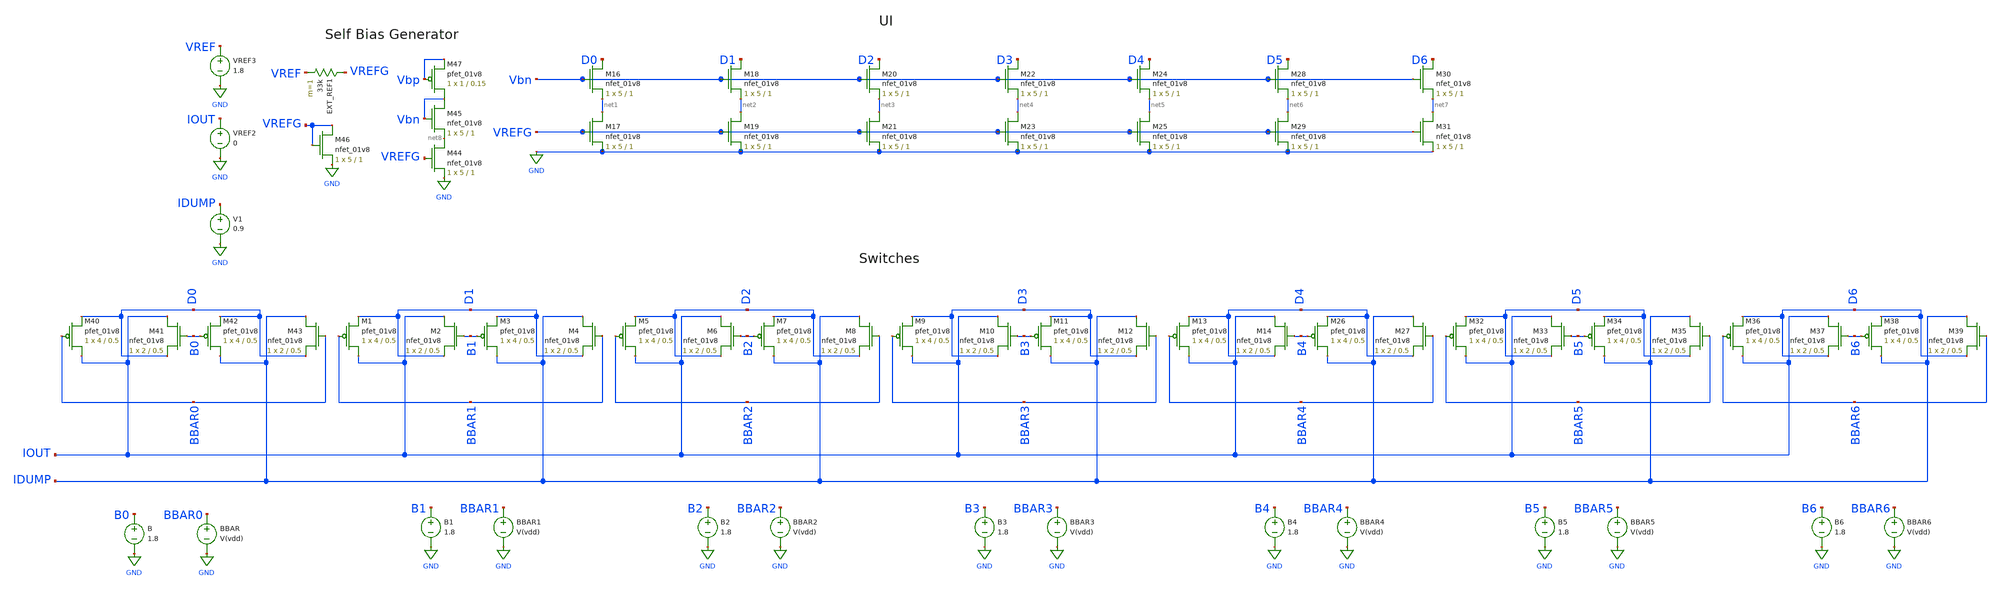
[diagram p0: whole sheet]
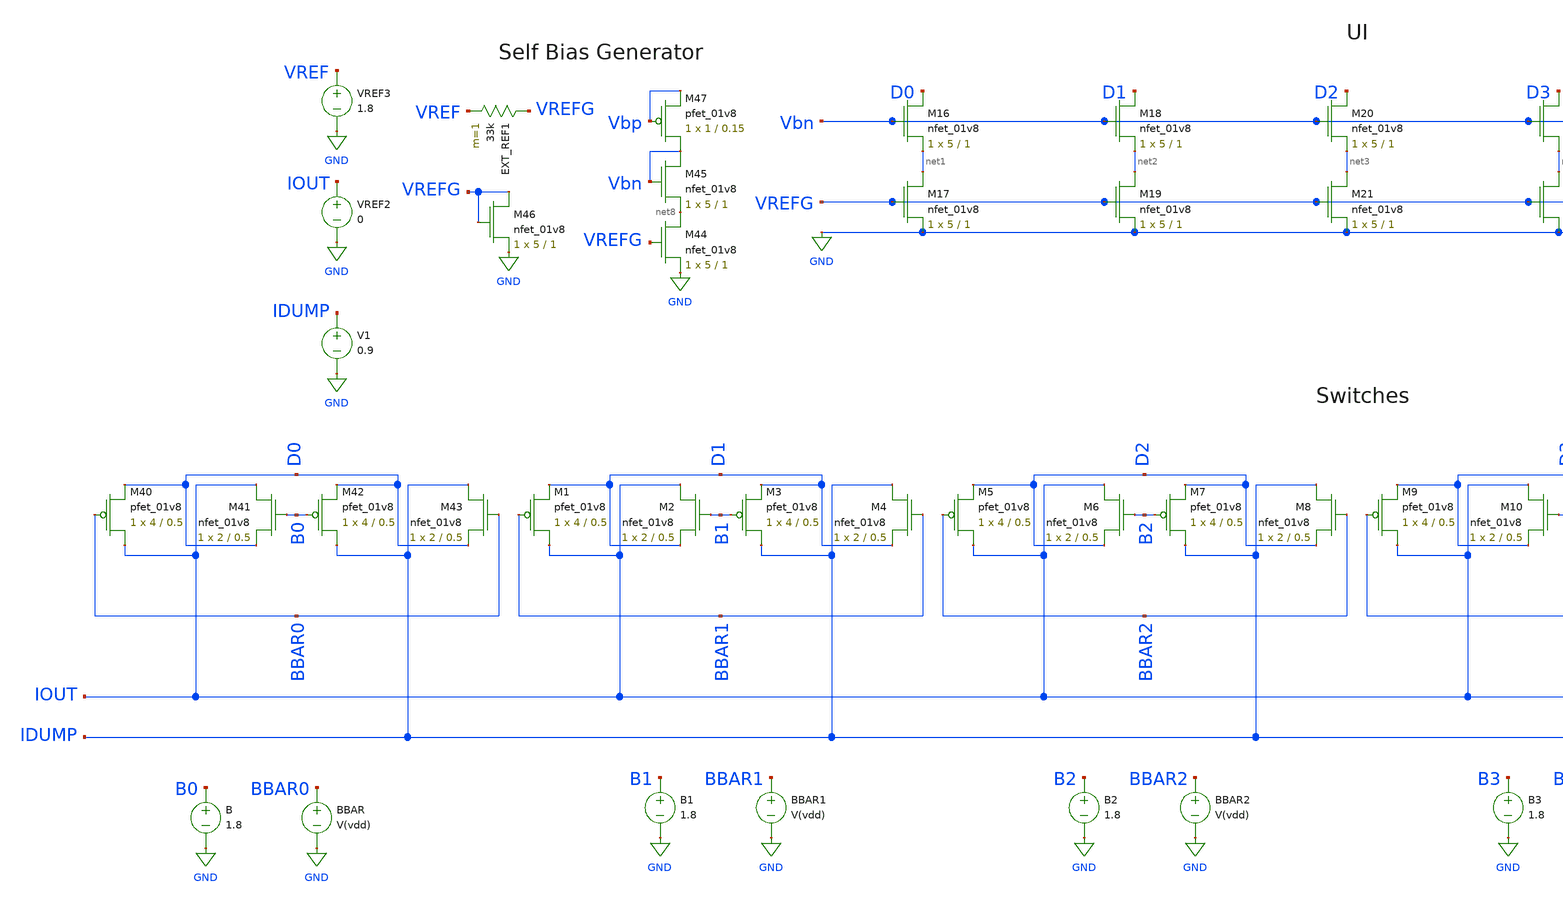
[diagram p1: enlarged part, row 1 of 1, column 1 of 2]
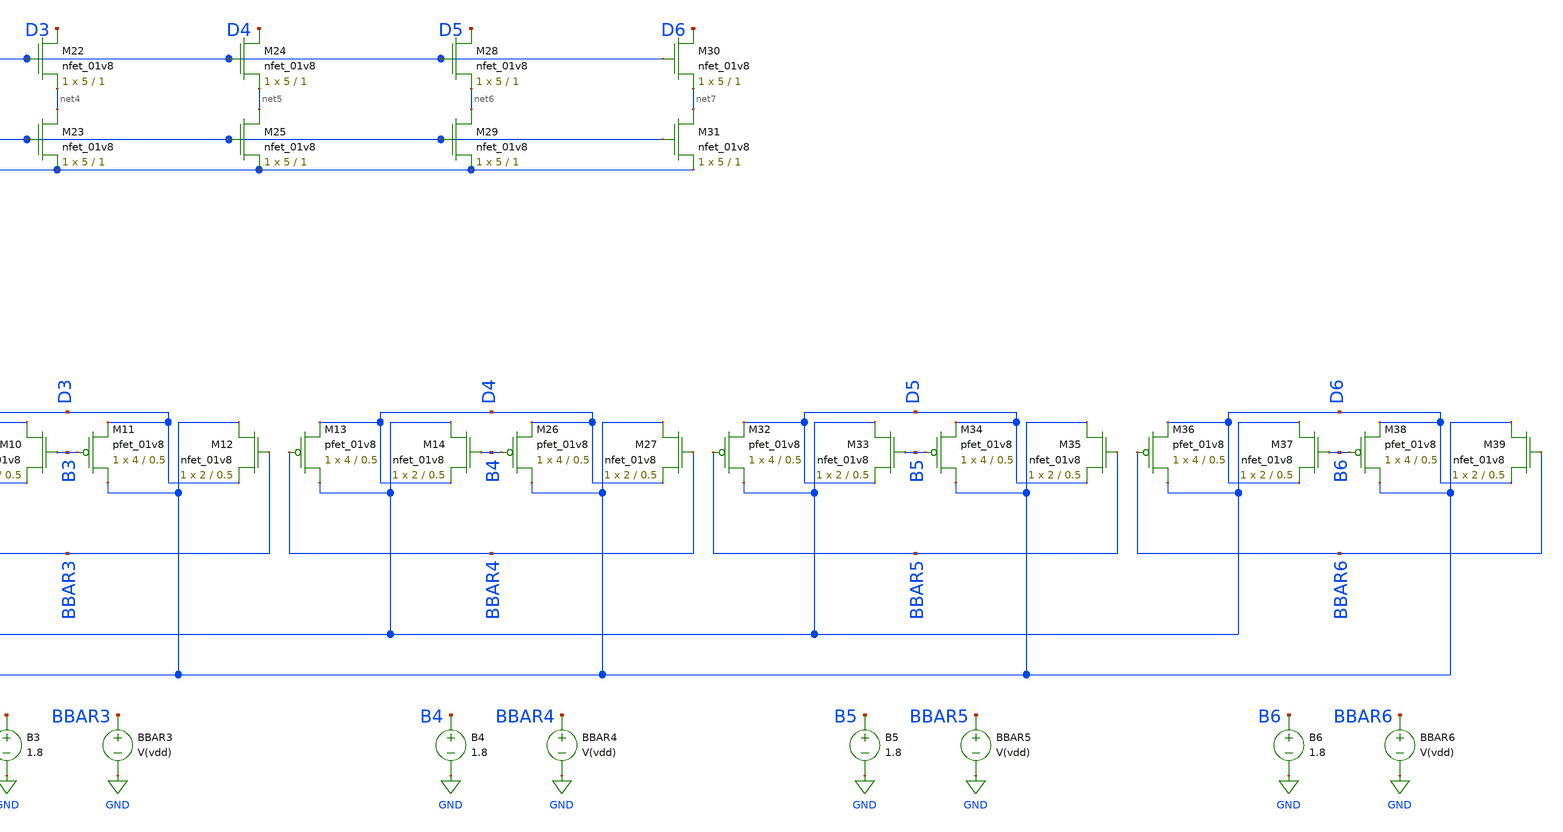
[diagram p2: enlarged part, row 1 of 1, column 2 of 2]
** sch_path: DAC2.sch
**.subckt DAC2
XM16 D0 Vbn net1 GND sky130_fd_pr__nfet_01v8 L=1 W=5 nf=1 ad='int((nf+1)/2) * W/nf * 0.29' as='int((nf+2)/2) * W/nf * 0.29'
+ pd='2*int((nf+1)/2) * (W/nf + 0.29)' ps='2*int((nf+2)/2) * (W/nf + 0.29)' nrd='0.29 / W' nrs='0.29 / W'
+ sa=0 sb=0 sd=0 mult=1 m=1
XM17 net1 VREFG GND GND sky130_fd_pr__nfet_01v8 L=1 W=5 nf=1 ad='int((nf+1)/2) * W/nf * 0.29' as='int((nf+2)/2) * W/nf * 0.29'
+ pd='2*int((nf+1)/2) * (W/nf + 0.29)' ps='2*int((nf+2)/2) * (W/nf + 0.29)' nrd='0.29 / W' nrs='0.29 / W'
+ sa=0 sb=0 sd=0 mult=1 m=1
XM18 D1 Vbn net2 GND sky130_fd_pr__nfet_01v8 L=1 W=5 nf=1 ad='int((nf+1)/2) * W/nf * 0.29' as='int((nf+2)/2) * W/nf * 0.29'
+ pd='2*int((nf+1)/2) * (W/nf + 0.29)' ps='2*int((nf+2)/2) * (W/nf + 0.29)' nrd='0.29 / W' nrs='0.29 / W'
+ sa=0 sb=0 sd=0 mult=1 m=1
XM19 net2 VREFG GND GND sky130_fd_pr__nfet_01v8 L=1 W=5 nf=1 ad='int((nf+1)/2) * W/nf * 0.29' as='int((nf+2)/2) * W/nf * 0.29'
+ pd='2*int((nf+1)/2) * (W/nf + 0.29)' ps='2*int((nf+2)/2) * (W/nf + 0.29)' nrd='0.29 / W' nrs='0.29 / W'
+ sa=0 sb=0 sd=0 mult=1 m=1
XM20 D2 Vbn net3 GND sky130_fd_pr__nfet_01v8 L=1 W=5 nf=1 ad='int((nf+1)/2) * W/nf * 0.29' as='int((nf+2)/2) * W/nf * 0.29'
+ pd='2*int((nf+1)/2) * (W/nf + 0.29)' ps='2*int((nf+2)/2) * (W/nf + 0.29)' nrd='0.29 / W' nrs='0.29 / W'
+ sa=0 sb=0 sd=0 mult=1 m=1
XM21 net3 VREFG GND GND sky130_fd_pr__nfet_01v8 L=1 W=5 nf=1 ad='int((nf+1)/2) * W/nf * 0.29' as='int((nf+2)/2) * W/nf * 0.29'
+ pd='2*int((nf+1)/2) * (W/nf + 0.29)' ps='2*int((nf+2)/2) * (W/nf + 0.29)' nrd='0.29 / W' nrs='0.29 / W'
+ sa=0 sb=0 sd=0 mult=1 m=1
XM22 D3 Vbn net4 GND sky130_fd_pr__nfet_01v8 L=1 W=5 nf=1 ad='int((nf+1)/2) * W/nf * 0.29' as='int((nf+2)/2) * W/nf * 0.29'
+ pd='2*int((nf+1)/2) * (W/nf + 0.29)' ps='2*int((nf+2)/2) * (W/nf + 0.29)' nrd='0.29 / W' nrs='0.29 / W'
+ sa=0 sb=0 sd=0 mult=1 m=1
XM23 net4 VREFG GND GND sky130_fd_pr__nfet_01v8 L=1 W=5 nf=1 ad='int((nf+1)/2) * W/nf * 0.29' as='int((nf+2)/2) * W/nf * 0.29'
+ pd='2*int((nf+1)/2) * (W/nf + 0.29)' ps='2*int((nf+2)/2) * (W/nf + 0.29)' nrd='0.29 / W' nrs='0.29 / W'
+ sa=0 sb=0 sd=0 mult=1 m=1
XM24 D4 Vbn net5 GND sky130_fd_pr__nfet_01v8 L=1 W=5 nf=1 ad='int((nf+1)/2) * W/nf * 0.29' as='int((nf+2)/2) * W/nf * 0.29'
+ pd='2*int((nf+1)/2) * (W/nf + 0.29)' ps='2*int((nf+2)/2) * (W/nf + 0.29)' nrd='0.29 / W' nrs='0.29 / W'
+ sa=0 sb=0 sd=0 mult=1 m=1
XM25 net5 VREFG GND GND sky130_fd_pr__nfet_01v8 L=1 W=5 nf=1 ad='int((nf+1)/2) * W/nf * 0.29' as='int((nf+2)/2) * W/nf * 0.29'
+ pd='2*int((nf+1)/2) * (W/nf + 0.29)' ps='2*int((nf+2)/2) * (W/nf + 0.29)' nrd='0.29 / W' nrs='0.29 / W'
+ sa=0 sb=0 sd=0 mult=1 m=1
XM28 D5 Vbn net6 GND sky130_fd_pr__nfet_01v8 L=1 W=5 nf=1 ad='int((nf+1)/2) * W/nf * 0.29' as='int((nf+2)/2) * W/nf * 0.29'
+ pd='2*int((nf+1)/2) * (W/nf + 0.29)' ps='2*int((nf+2)/2) * (W/nf + 0.29)' nrd='0.29 / W' nrs='0.29 / W'
+ sa=0 sb=0 sd=0 mult=1 m=1
XM29 net6 VREFG GND GND sky130_fd_pr__nfet_01v8 L=1 W=5 nf=1 ad='int((nf+1)/2) * W/nf * 0.29' as='int((nf+2)/2) * W/nf * 0.29'
+ pd='2*int((nf+1)/2) * (W/nf + 0.29)' ps='2*int((nf+2)/2) * (W/nf + 0.29)' nrd='0.29 / W' nrs='0.29 / W'
+ sa=0 sb=0 sd=0 mult=1 m=1
XM30 D6 Vbn net7 GND sky130_fd_pr__nfet_01v8 L=1 W=5 nf=1 ad='int((nf+1)/2) * W/nf * 0.29' as='int((nf+2)/2) * W/nf * 0.29'
+ pd='2*int((nf+1)/2) * (W/nf + 0.29)' ps='2*int((nf+2)/2) * (W/nf + 0.29)' nrd='0.29 / W' nrs='0.29 / W'
+ sa=0 sb=0 sd=0 mult=1 m=1
XM31 net7 VREFG GND GND sky130_fd_pr__nfet_01v8 L=1 W=5 nf=1 ad='int((nf+1)/2) * W/nf * 0.29' as='int((nf+2)/2) * W/nf * 0.29'
+ pd='2*int((nf+1)/2) * (W/nf + 0.29)' ps='2*int((nf+2)/2) * (W/nf + 0.29)' nrd='0.29 / W' nrs='0.29 / W'
+ sa=0 sb=0 sd=0 mult=1 m=1
VREF2 IOUT GND 0
XM1 IOUT BBAR1 D1 VDD sky130_fd_pr__pfet_01v8 L=0.5 W=4 nf=1 ad='int((nf+1)/2) * W/nf * 0.29' as='int((nf+2)/2) * W/nf * 0.29'
+ pd='2*int((nf+1)/2) * (W/nf + 0.29)' ps='2*int((nf+2)/2) * (W/nf + 0.29)' nrd='0.29 / W' nrs='0.29 / W'
+ sa=0 sb=0 sd=0 mult=1 m=1
XM2 IOUT B1 D1 GND sky130_fd_pr__nfet_01v8 L=0.5 W=2 nf=1 ad='int((nf+1)/2) * W/nf * 0.29' as='int((nf+2)/2) * W/nf * 0.29'
+ pd='2*int((nf+1)/2) * (W/nf + 0.29)' ps='2*int((nf+2)/2) * (W/nf + 0.29)' nrd='0.29 / W' nrs='0.29 / W'
+ sa=0 sb=0 sd=0 mult=1 m=1
XM3 IDUMP B1 D1 VDD sky130_fd_pr__pfet_01v8 L=0.5 W=4 nf=1 ad='int((nf+1)/2) * W/nf * 0.29' as='int((nf+2)/2) * W/nf * 0.29'
+ pd='2*int((nf+1)/2) * (W/nf + 0.29)' ps='2*int((nf+2)/2) * (W/nf + 0.29)' nrd='0.29 / W' nrs='0.29 / W'
+ sa=0 sb=0 sd=0 mult=1 m=1
XM4 IDUMP BBAR1 D1 GND sky130_fd_pr__nfet_01v8 L=0.5 W=2 nf=1 ad='int((nf+1)/2) * W/nf * 0.29' as='int((nf+2)/2) * W/nf * 0.29'
+ pd='2*int((nf+1)/2) * (W/nf + 0.29)' ps='2*int((nf+2)/2) * (W/nf + 0.29)' nrd='0.29 / W' nrs='0.29 / W'
+ sa=0 sb=0 sd=0 mult=1 m=1
V1 IDUMP GND 0.9
XM5 IOUT BBAR2 D2 VDD sky130_fd_pr__pfet_01v8 L=0.5 W=4 nf=1 ad='int((nf+1)/2) * W/nf * 0.29' as='int((nf+2)/2) * W/nf * 0.29'
+ pd='2*int((nf+1)/2) * (W/nf + 0.29)' ps='2*int((nf+2)/2) * (W/nf + 0.29)' nrd='0.29 / W' nrs='0.29 / W'
+ sa=0 sb=0 sd=0 mult=1 m=1
XM6 IOUT B2 D2 GND sky130_fd_pr__nfet_01v8 L=0.5 W=2 nf=1 ad='int((nf+1)/2) * W/nf * 0.29' as='int((nf+2)/2) * W/nf * 0.29'
+ pd='2*int((nf+1)/2) * (W/nf + 0.29)' ps='2*int((nf+2)/2) * (W/nf + 0.29)' nrd='0.29 / W' nrs='0.29 / W'
+ sa=0 sb=0 sd=0 mult=1 m=1
XM7 IDUMP B2 D2 VDD sky130_fd_pr__pfet_01v8 L=0.5 W=4 nf=1 ad='int((nf+1)/2) * W/nf * 0.29' as='int((nf+2)/2) * W/nf * 0.29'
+ pd='2*int((nf+1)/2) * (W/nf + 0.29)' ps='2*int((nf+2)/2) * (W/nf + 0.29)' nrd='0.29 / W' nrs='0.29 / W'
+ sa=0 sb=0 sd=0 mult=1 m=1
XM8 IDUMP BBAR2 D2 GND sky130_fd_pr__nfet_01v8 L=0.5 W=2 nf=1 ad='int((nf+1)/2) * W/nf * 0.29' as='int((nf+2)/2) * W/nf * 0.29'
+ pd='2*int((nf+1)/2) * (W/nf + 0.29)' ps='2*int((nf+2)/2) * (W/nf + 0.29)' nrd='0.29 / W' nrs='0.29 / W'
+ sa=0 sb=0 sd=0 mult=1 m=1
XM9 IOUT BBAR3 D3 VDD sky130_fd_pr__pfet_01v8 L=0.5 W=4 nf=1 ad='int((nf+1)/2) * W/nf * 0.29' as='int((nf+2)/2) * W/nf * 0.29'
+ pd='2*int((nf+1)/2) * (W/nf + 0.29)' ps='2*int((nf+2)/2) * (W/nf + 0.29)' nrd='0.29 / W' nrs='0.29 / W'
+ sa=0 sb=0 sd=0 mult=1 m=1
XM10 IOUT B3 D3 GND sky130_fd_pr__nfet_01v8 L=0.5 W=2 nf=1 ad='int((nf+1)/2) * W/nf * 0.29' as='int((nf+2)/2) * W/nf * 0.29'
+ pd='2*int((nf+1)/2) * (W/nf + 0.29)' ps='2*int((nf+2)/2) * (W/nf + 0.29)' nrd='0.29 / W' nrs='0.29 / W'
+ sa=0 sb=0 sd=0 mult=1 m=1
XM11 IDUMP B3 D3 VDD sky130_fd_pr__pfet_01v8 L=0.5 W=4 nf=1 ad='int((nf+1)/2) * W/nf * 0.29' as='int((nf+2)/2) * W/nf * 0.29'
+ pd='2*int((nf+1)/2) * (W/nf + 0.29)' ps='2*int((nf+2)/2) * (W/nf + 0.29)' nrd='0.29 / W' nrs='0.29 / W'
+ sa=0 sb=0 sd=0 mult=1 m=1
XM12 IDUMP BBAR3 D3 GND sky130_fd_pr__nfet_01v8 L=0.5 W=2 nf=1 ad='int((nf+1)/2) * W/nf * 0.29' as='int((nf+2)/2) * W/nf * 0.29'
+ pd='2*int((nf+1)/2) * (W/nf + 0.29)' ps='2*int((nf+2)/2) * (W/nf + 0.29)' nrd='0.29 / W' nrs='0.29 / W'
+ sa=0 sb=0 sd=0 mult=1 m=1
XM13 IOUT BBAR4 D4 VDD sky130_fd_pr__pfet_01v8 L=0.5 W=4 nf=1 ad='int((nf+1)/2) * W/nf * 0.29' as='int((nf+2)/2) * W/nf * 0.29'
+ pd='2*int((nf+1)/2) * (W/nf + 0.29)' ps='2*int((nf+2)/2) * (W/nf + 0.29)' nrd='0.29 / W' nrs='0.29 / W'
+ sa=0 sb=0 sd=0 mult=1 m=1
XM14 IOUT B4 D4 GND sky130_fd_pr__nfet_01v8 L=0.5 W=2 nf=1 ad='int((nf+1)/2) * W/nf * 0.29' as='int((nf+2)/2) * W/nf * 0.29'
+ pd='2*int((nf+1)/2) * (W/nf + 0.29)' ps='2*int((nf+2)/2) * (W/nf + 0.29)' nrd='0.29 / W' nrs='0.29 / W'
+ sa=0 sb=0 sd=0 mult=1 m=1
XM26 IDUMP B4 D4 VDD sky130_fd_pr__pfet_01v8 L=0.5 W=4 nf=1 ad='int((nf+1)/2) * W/nf * 0.29' as='int((nf+2)/2) * W/nf * 0.29'
+ pd='2*int((nf+1)/2) * (W/nf + 0.29)' ps='2*int((nf+2)/2) * (W/nf + 0.29)' nrd='0.29 / W' nrs='0.29 / W'
+ sa=0 sb=0 sd=0 mult=1 m=1
XM27 IDUMP BBAR4 D4 GND sky130_fd_pr__nfet_01v8 L=0.5 W=2 nf=1 ad='int((nf+1)/2) * W/nf * 0.29' as='int((nf+2)/2) * W/nf * 0.29'
+ pd='2*int((nf+1)/2) * (W/nf + 0.29)' ps='2*int((nf+2)/2) * (W/nf + 0.29)' nrd='0.29 / W' nrs='0.29 / W'
+ sa=0 sb=0 sd=0 mult=1 m=1
XM32 IOUT BBAR5 D5 VDD sky130_fd_pr__pfet_01v8 L=0.5 W=4 nf=1 ad='int((nf+1)/2) * W/nf * 0.29' as='int((nf+2)/2) * W/nf * 0.29'
+ pd='2*int((nf+1)/2) * (W/nf + 0.29)' ps='2*int((nf+2)/2) * (W/nf + 0.29)' nrd='0.29 / W' nrs='0.29 / W'
+ sa=0 sb=0 sd=0 mult=1 m=1
XM33 IOUT B5 D5 GND sky130_fd_pr__nfet_01v8 L=0.5 W=2 nf=1 ad='int((nf+1)/2) * W/nf * 0.29' as='int((nf+2)/2) * W/nf * 0.29'
+ pd='2*int((nf+1)/2) * (W/nf + 0.29)' ps='2*int((nf+2)/2) * (W/nf + 0.29)' nrd='0.29 / W' nrs='0.29 / W'
+ sa=0 sb=0 sd=0 mult=1 m=1
XM34 IDUMP B5 D5 VDD sky130_fd_pr__pfet_01v8 L=0.5 W=4 nf=1 ad='int((nf+1)/2) * W/nf * 0.29' as='int((nf+2)/2) * W/nf * 0.29'
+ pd='2*int((nf+1)/2) * (W/nf + 0.29)' ps='2*int((nf+2)/2) * (W/nf + 0.29)' nrd='0.29 / W' nrs='0.29 / W'
+ sa=0 sb=0 sd=0 mult=1 m=1
XM35 IDUMP BBAR5 D5 GND sky130_fd_pr__nfet_01v8 L=0.5 W=2 nf=1 ad='int((nf+1)/2) * W/nf * 0.29' as='int((nf+2)/2) * W/nf * 0.29'
+ pd='2*int((nf+1)/2) * (W/nf + 0.29)' ps='2*int((nf+2)/2) * (W/nf + 0.29)' nrd='0.29 / W' nrs='0.29 / W'
+ sa=0 sb=0 sd=0 mult=1 m=1
XM36 IOUT BBAR6 D6 VDD sky130_fd_pr__pfet_01v8 L=0.5 W=4 nf=1 ad='int((nf+1)/2) * W/nf * 0.29' as='int((nf+2)/2) * W/nf * 0.29'
+ pd='2*int((nf+1)/2) * (W/nf + 0.29)' ps='2*int((nf+2)/2) * (W/nf + 0.29)' nrd='0.29 / W' nrs='0.29 / W'
+ sa=0 sb=0 sd=0 mult=1 m=1
XM37 IOUT B6 D6 GND sky130_fd_pr__nfet_01v8 L=0.5 W=2 nf=1 ad='int((nf+1)/2) * W/nf * 0.29' as='int((nf+2)/2) * W/nf * 0.29'
+ pd='2*int((nf+1)/2) * (W/nf + 0.29)' ps='2*int((nf+2)/2) * (W/nf + 0.29)' nrd='0.29 / W' nrs='0.29 / W'
+ sa=0 sb=0 sd=0 mult=1 m=1
XM38 IDUMP B6 D6 VDD sky130_fd_pr__pfet_01v8 L=0.5 W=4 nf=1 ad='int((nf+1)/2) * W/nf * 0.29' as='int((nf+2)/2) * W/nf * 0.29'
+ pd='2*int((nf+1)/2) * (W/nf + 0.29)' ps='2*int((nf+2)/2) * (W/nf + 0.29)' nrd='0.29 / W' nrs='0.29 / W'
+ sa=0 sb=0 sd=0 mult=1 m=1
XM39 IDUMP BBAR6 D6 GND sky130_fd_pr__nfet_01v8 L=0.5 W=2 nf=1 ad='int((nf+1)/2) * W/nf * 0.29' as='int((nf+2)/2) * W/nf * 0.29'
+ pd='2*int((nf+1)/2) * (W/nf + 0.29)' ps='2*int((nf+2)/2) * (W/nf + 0.29)' nrd='0.29 / W' nrs='0.29 / W'
+ sa=0 sb=0 sd=0 mult=1 m=1
XM40 IOUT BBAR0 D0 VDD sky130_fd_pr__pfet_01v8 L=0.5 W=4 nf=1 ad='int((nf+1)/2) * W/nf * 0.29' as='int((nf+2)/2) * W/nf * 0.29'
+ pd='2*int((nf+1)/2) * (W/nf + 0.29)' ps='2*int((nf+2)/2) * (W/nf + 0.29)' nrd='0.29 / W' nrs='0.29 / W'
+ sa=0 sb=0 sd=0 mult=1 m=1
XM41 IOUT B0 D0 GND sky130_fd_pr__nfet_01v8 L=0.5 W=2 nf=1 ad='int((nf+1)/2) * W/nf * 0.29' as='int((nf+2)/2) * W/nf * 0.29'
+ pd='2*int((nf+1)/2) * (W/nf + 0.29)' ps='2*int((nf+2)/2) * (W/nf + 0.29)' nrd='0.29 / W' nrs='0.29 / W'
+ sa=0 sb=0 sd=0 mult=1 m=1
XM42 IDUMP B0 D0 VDD sky130_fd_pr__pfet_01v8 L=0.5 W=4 nf=1 ad='int((nf+1)/2) * W/nf * 0.29' as='int((nf+2)/2) * W/nf * 0.29'
+ pd='2*int((nf+1)/2) * (W/nf + 0.29)' ps='2*int((nf+2)/2) * (W/nf + 0.29)' nrd='0.29 / W' nrs='0.29 / W'
+ sa=0 sb=0 sd=0 mult=1 m=1
XM43 IDUMP BBAR0 D0 GND sky130_fd_pr__nfet_01v8 L=0.5 W=2 nf=1 ad='int((nf+1)/2) * W/nf * 0.29' as='int((nf+2)/2) * W/nf * 0.29'
+ pd='2*int((nf+1)/2) * (W/nf + 0.29)' ps='2*int((nf+2)/2) * (W/nf + 0.29)' nrd='0.29 / W' nrs='0.29 / W'
+ sa=0 sb=0 sd=0 mult=1 m=1
B B0 GND 1.8
BBAR BBAR0 GND V(vdd)
B1 B1 GND 1.8
BBAR1 BBAR1 GND V(vdd)
B2 B2 GND 1.8
BBAR2 BBAR2 GND V(vdd)
B3 B3 GND 1.8
BBAR3 BBAR3 GND V(vdd)
B4 B4 GND 1.8
BBAR4 BBAR4 GND V(vdd)
B5 B5 GND 1.8
BBAR5 BBAR5 GND V(vdd)
B6 B6 GND 1.8
BBAR6 BBAR6 GND V(vdd)
XM44 net8 VREFG GND GND sky130_fd_pr__nfet_01v8 L=1 W=5 nf=1 ad='int((nf+1)/2) * W/nf * 0.29' as='int((nf+2)/2) * W/nf * 0.29'
+ pd='2*int((nf+1)/2) * (W/nf + 0.29)' ps='2*int((nf+2)/2) * (W/nf + 0.29)' nrd='0.29 / W' nrs='0.29 / W'
+ sa=0 sb=0 sd=0 mult=1 m=1
EXT_REF1 VREFG VREF 33k m=1
VREF3 VREF GND 1.8
XM45 Vbn Vbn net8 GND sky130_fd_pr__nfet_01v8 L=1 W=5 nf=1 ad='int((nf+1)/2) * W/nf * 0.29' as='int((nf+2)/2) * W/nf * 0.29'
+ pd='2*int((nf+1)/2) * (W/nf + 0.29)' ps='2*int((nf+2)/2) * (W/nf + 0.29)' nrd='0.29 / W' nrs='0.29 / W'
+ sa=0 sb=0 sd=0 mult=1 m=1
XM46 VREFG VREFG GND GND sky130_fd_pr__nfet_01v8 L=1 W=5 nf=1 ad='int((nf+1)/2) * W/nf * 0.29' as='int((nf+2)/2) * W/nf * 0.29'
+ pd='2*int((nf+1)/2) * (W/nf + 0.29)' ps='2*int((nf+2)/2) * (W/nf + 0.29)' nrd='0.29 / W' nrs='0.29 / W'
+ sa=0 sb=0 sd=0 mult=1 m=1
XM47 Vbn Vbp Vbp VDD sky130_fd_pr__pfet_01v8 L=0.15 W=1 nf=1 ad='int((nf+1)/2) * W/nf * 0.29' as='int((nf+2)/2) * W/nf * 0.29'
+ pd='2*int((nf+1)/2) * (W/nf + 0.29)' ps='2*int((nf+2)/2) * (W/nf + 0.29)' nrd='0.29 / W' nrs='0.29 / W'
+ sa=0 sb=0 sd=0 mult=1 m=1
**.ends
.GLOBAL GND
.end
